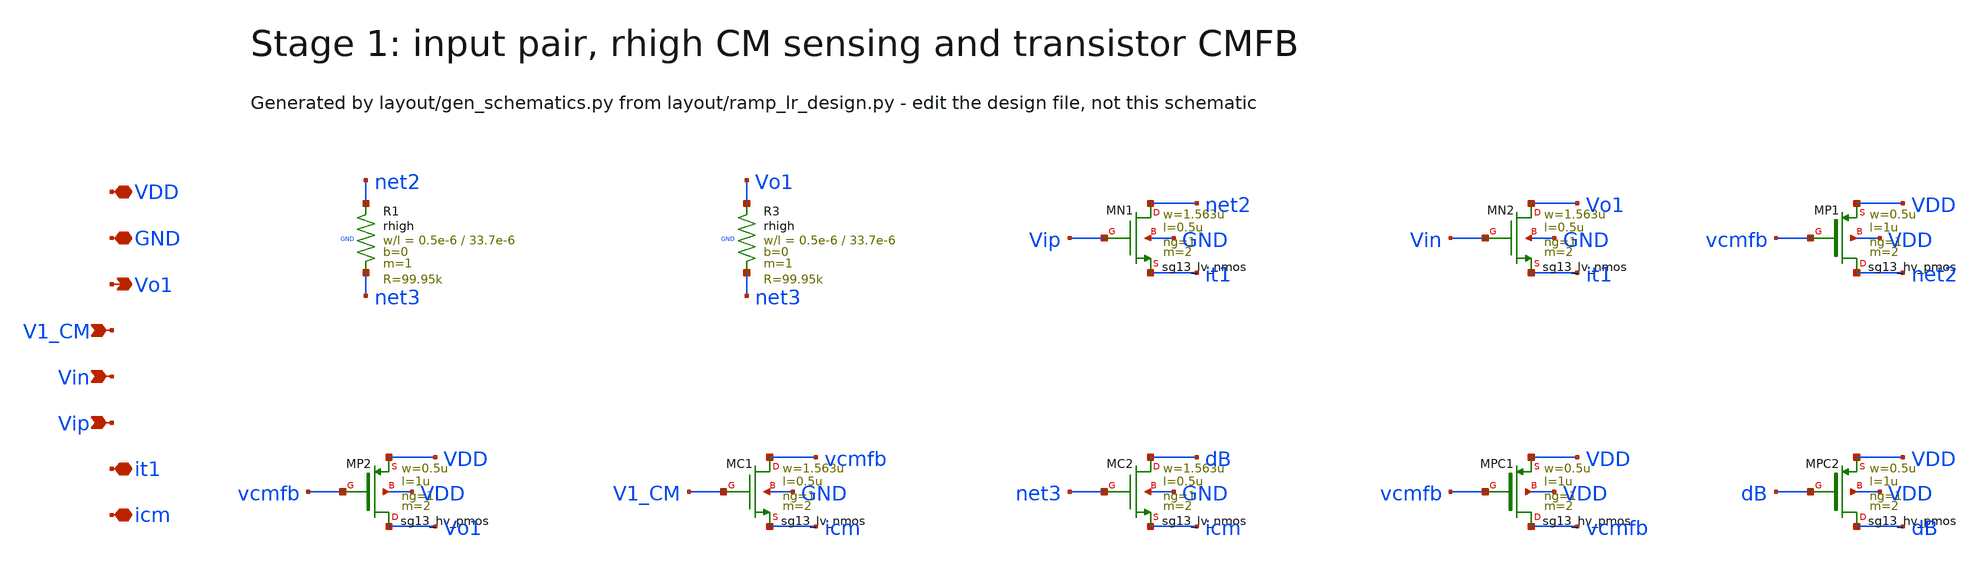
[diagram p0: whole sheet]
** sch_path: Design Files/RAMP/RAMP-LR/STG1_LR.sch
**.subckt STG1_LR VDD GND Vo1 V1_CM Vin Vip it1 icm
*.iopin VDD
*.iopin GND
*.opin Vo1
*.ipin V1_CM
*.ipin Vin
*.ipin Vip
*.iopin it1
*.iopin icm
XR1 net2 net3 GND rhigh w=0.5e-6 l=33.7e-6 m=1 b=0 mm_ok=1
XR3 Vo1 net3 GND rhigh w=0.5e-6 l=33.7e-6 m=1 b=0 mm_ok=1
XMN1 net2 Vip it1 GND sg13_lv_nmos w=1.563u l=0.5u ng=1 m=2 mm_ok=1
XMN2 Vo1 Vin it1 GND sg13_lv_nmos w=1.563u l=0.5u ng=1 m=2 mm_ok=1
XMP1 net2 vcmfb VDD VDD sg13_hv_pmos w=0.5u l=1u ng=1 m=2 mm_ok=1
XMP2 Vo1 vcmfb VDD VDD sg13_hv_pmos w=0.5u l=1u ng=1 m=2 mm_ok=1
XMC1 vcmfb V1_CM icm GND sg13_lv_nmos w=1.563u l=0.5u ng=1 m=2 mm_ok=1
XMC2 dB net3 icm GND sg13_lv_nmos w=1.563u l=0.5u ng=1 m=2 mm_ok=1
XMPC1 vcmfb vcmfb VDD VDD sg13_hv_pmos w=0.5u l=1u ng=1 m=2 mm_ok=1
XMPC2 dB dB VDD VDD sg13_hv_pmos w=0.5u l=1u ng=1 m=2 mm_ok=1
**.ends
.end
